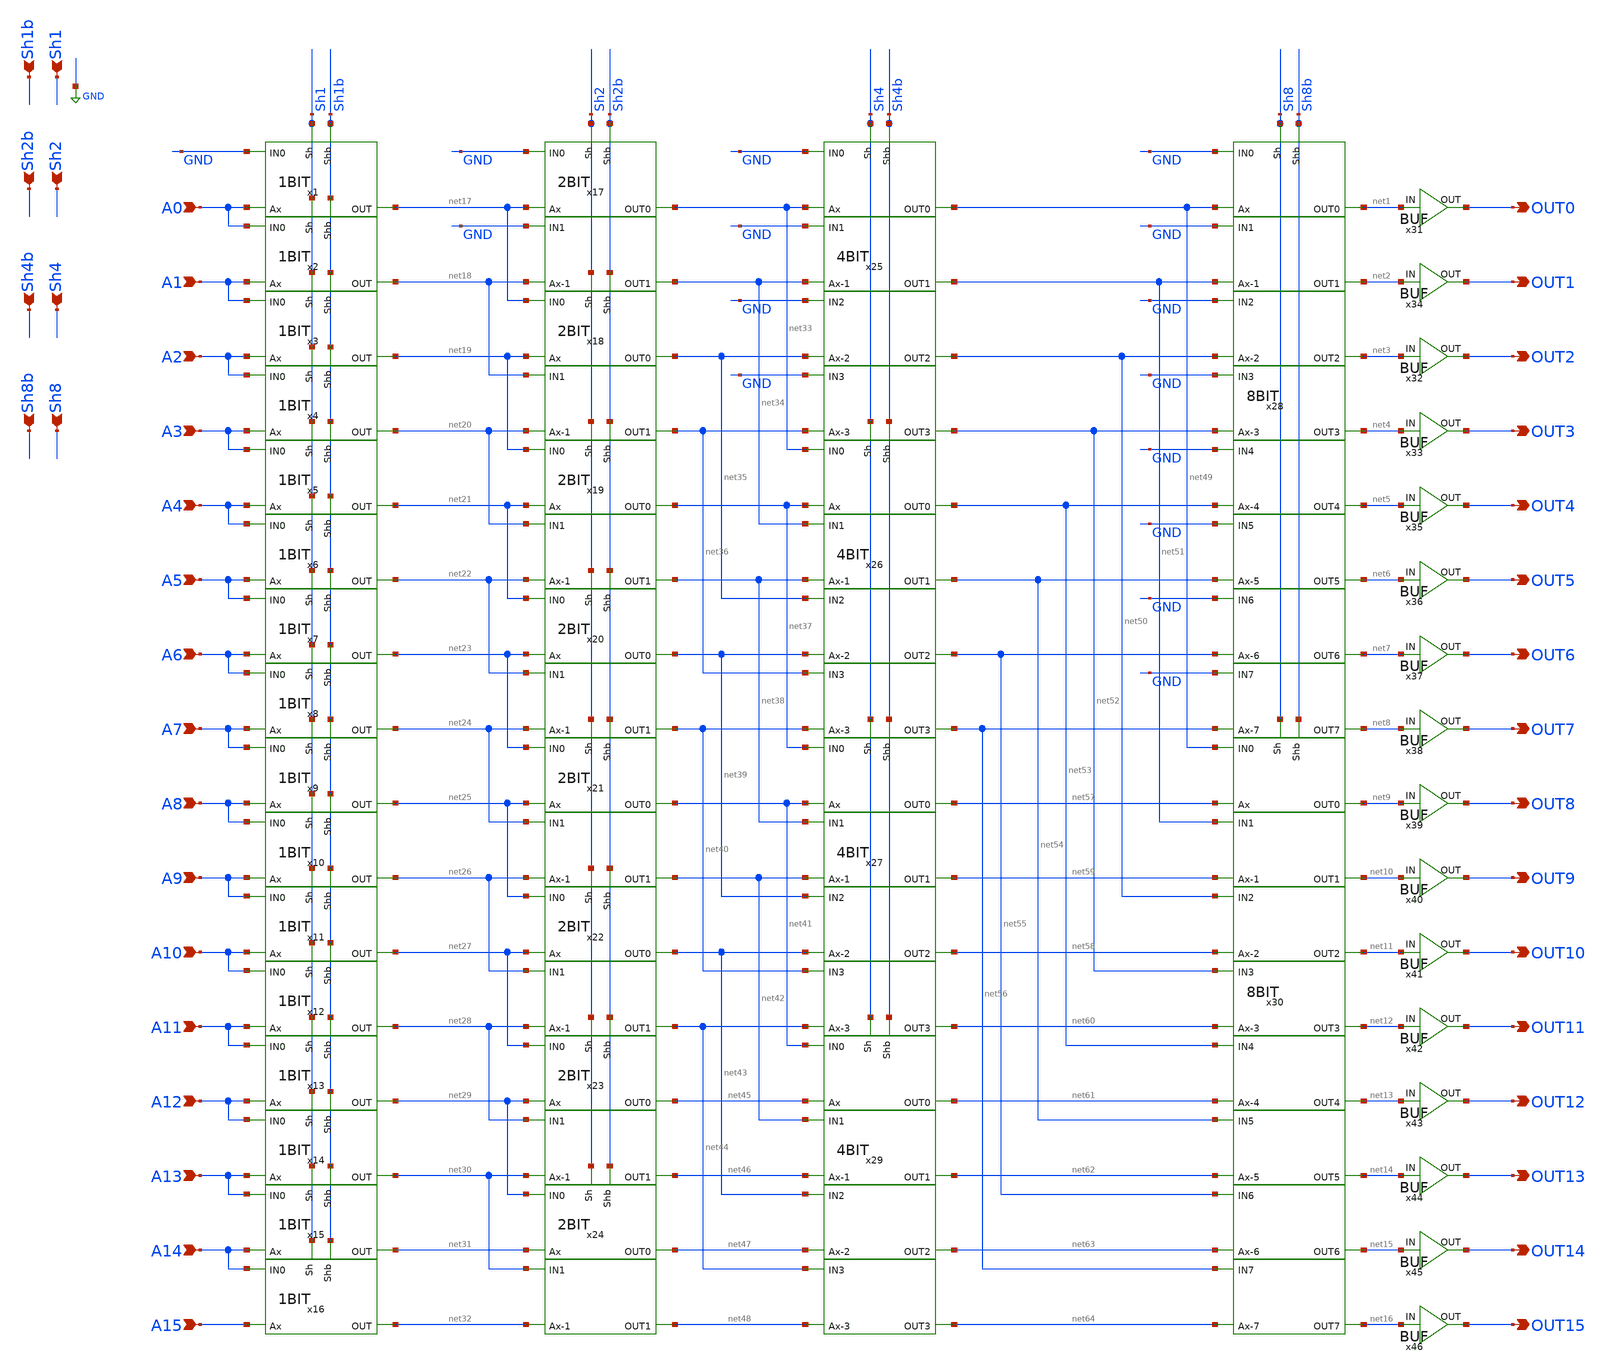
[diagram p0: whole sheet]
** sch_path: SHIFT.sch
**.subckt SHIFT Sh1 Sh1b A0 A1 A2 A3 A4 A5 A6 A7 A8 A9 A10 A11 A12 A13 A14 A15 OUT0 OUT1 OUT2 OUT3
*+ OUT4 OUT5 OUT6 OUT7 OUT8 OUT9 OUT10 OUT11 OUT12 OUT13 OUT14 OUT15 Sh2 Sh2b Sh4 Sh4b Sh8 Sh8b
*.ipin Sh1
*.ipin Sh1b
*.ipin A0
*.ipin A1
*.ipin A2
*.ipin A3
*.ipin A4
*.ipin A5
*.ipin A6
*.ipin A7
*.ipin A8
*.ipin A9
*.ipin A10
*.ipin A11
*.ipin A12
*.ipin A13
*.ipin A14
*.ipin A15
*.opin OUT0
*.opin OUT1
*.opin OUT2
*.opin OUT3
*.opin OUT4
*.opin OUT5
*.opin OUT6
*.opin OUT7
*.opin OUT8
*.opin OUT9
*.opin OUT10
*.opin OUT11
*.opin OUT12
*.opin OUT13
*.opin OUT14
*.opin OUT15
*.ipin Sh2
*.ipin Sh2b
*.ipin Sh4
*.ipin Sh4b
*.ipin Sh8
*.ipin Sh8b
x1 Sh1b Sh1 A0 GND net17 1BIT
x2 Sh1b Sh1 A1 A0 net18 1BIT
x3 Sh1b Sh1 A2 A1 net19 1BIT
x4 Sh1b Sh1 A3 A2 net20 1BIT
x5 Sh1b Sh1 A4 A3 net21 1BIT
x6 Sh1b Sh1 A5 A4 net22 1BIT
x7 Sh1b Sh1 A6 A5 net23 1BIT
x8 Sh1b Sh1 A7 A6 net24 1BIT
x9 Sh1b Sh1 A8 A7 net25 1BIT
x10 Sh1b Sh1 A9 A8 net26 1BIT
x11 Sh1b Sh1 A10 A9 net27 1BIT
x12 Sh1b Sh1 A11 A10 net28 1BIT
x13 Sh1b Sh1 A12 A11 net29 1BIT
x14 Sh1b Sh1 A13 A12 net30 1BIT
x15 Sh1b Sh1 A14 A13 net31 1BIT
x16 Sh1b Sh1 A15 A14 net32 1BIT
x17 Sh2b Sh2 net17 GND net33 net34 GND net18 2BIT
x18 Sh2b Sh2 net19 net17 net35 net36 net18 net20 2BIT
x19 Sh2b Sh2 net21 net19 net37 net38 net20 net22 2BIT
x20 Sh2b Sh2 net23 net21 net39 net40 net22 net24 2BIT
x21 Sh2b Sh2 net25 net23 net41 net42 net24 net26 2BIT
x22 Sh2b Sh2 net27 net25 net43 net44 net26 net28 2BIT
x23 Sh2b Sh2 net29 net27 net45 net46 net28 net30 2BIT
x24 Sh2b Sh2 net31 net29 net47 net48 net30 net32 2BIT
x25 Sh4b Sh4 GND net33 net49 net51 net50 net52 GND net34 GND net35 GND net36 4BIT
x26 Sh4b Sh4 net33 net37 net53 net54 net55 net56 net34 net38 net35 net39 net36 net40 4BIT
x27 Sh4b Sh4 net37 net41 net57 net59 net58 net60 net38 net42 net39 net43 net40 net44 4BIT
x29 Sh4b Sh4 net41 net45 net61 net62 net63 net64 net42 net46 net43 net47 net44 net48 4BIT
x28 Sh8b Sh8 net49 GND net1 net2 net3 net4 net51 GND GND net50 GND net52 net53 GND net5 net6 net7
+ net8 GND net54 GND net55 GND net56 8BIT
x30 Sh8b Sh8 net57 net49 net9 net10 net11 net12 net59 net51 net50 net58 net52 net60 net61 net53
+ net13 net14 net15 net16 net54 net62 net55 net63 net56 net64 8BIT
x31 OUT0 net1 BUF
x32 OUT2 net3 BUF
x33 OUT3 net4 BUF
x34 OUT1 net2 BUF
x35 OUT4 net5 BUF
x36 OUT5 net6 BUF
x37 OUT6 net7 BUF
x38 OUT7 net8 BUF
x39 OUT8 net9 BUF
x40 OUT9 net10 BUF
x41 OUT10 net11 BUF
x42 OUT11 net12 BUF
x43 OUT12 net13 BUF
x44 OUT13 net14 BUF
x45 OUT14 net15 BUF
x46 OUT15 net16 BUF
**.ends
.GLOBAL GND
.end
